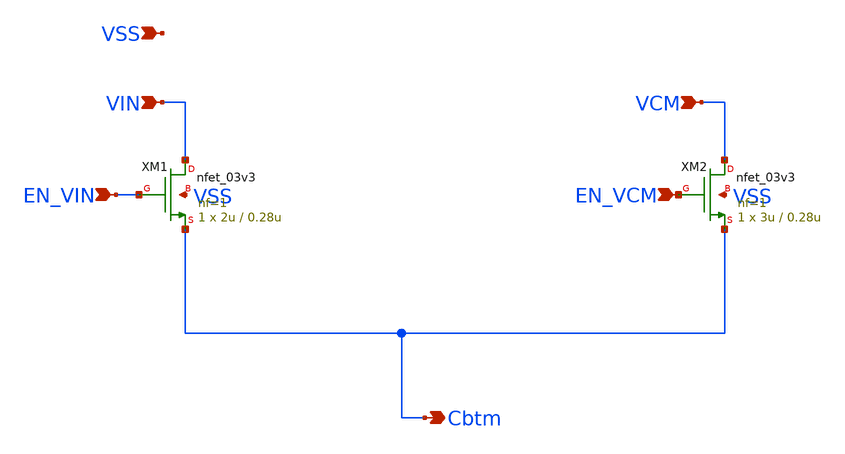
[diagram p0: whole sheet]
** sch_path: Schematic/individual_switch/switch_C0_dummy.sch
**.subckt switch_C0_dummy VIN EN_VIN VCM EN_VCM Cbtm VSS
*.ipin VIN
*.ipin EN_VIN
*.ipin VCM
*.ipin EN_VCM
*.opin Cbtm
*.ipin VSS
XM1 VIN EN_VIN Cbtm VSS nfet_03v3 L=0.28u W=2u nf=1 ad='int((nf+1)/2) * W/nf * 0.18u' as='int((nf+2)/2) * W/nf * 0.18u'
+ pd='2*int((nf+1)/2) * (W/nf + 0.18u)' ps='2*int((nf+2)/2) * (W/nf + 0.18u)' nrd='0.18u / W' nrs='0.18u / W'
+ sa=0 sb=0 sd=0 m=1
XM2 VCM EN_VCM Cbtm VSS nfet_03v3 L=0.28u W=3u nf=1 ad='int((nf+1)/2) * W/nf * 0.18u' as='int((nf+2)/2) * W/nf * 0.18u'
+ pd='2*int((nf+1)/2) * (W/nf + 0.18u)' ps='2*int((nf+2)/2) * (W/nf + 0.18u)' nrd='0.18u / W' nrs='0.18u / W'
+ sa=0 sb=0 sd=0 m=1
**.ends
.end
